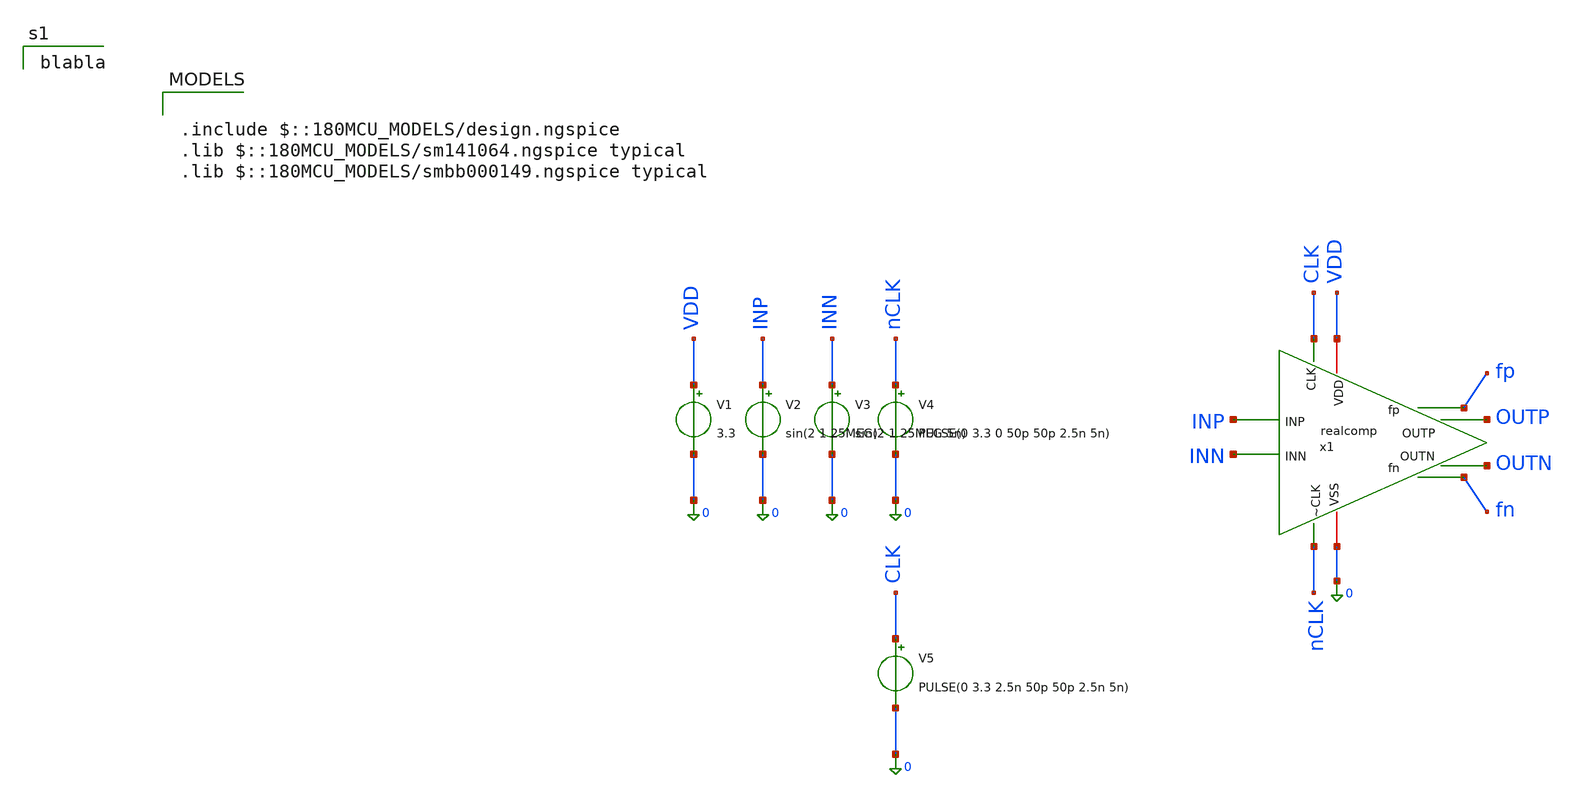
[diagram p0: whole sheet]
** sch_path: analog/blocks/Double_Tail_Comparator/realcomptest.sch
**.subckt realcomptest
V1 VDD 0 3.3
V2 INP 0 sin(2 1 25MEG)
V3 INN 0 sin(2 1 25MEG 5n)
V4 nCLK 0 PULSE(0 3.3 0 50p 50p 2.5n 5n)
V5 CLK 0 PULSE(0 3.3 2.5n 50p 50p 2.5n 5n)
x1 nCLK OUTN OUTP CLK VDD 0 fp fn INP INN realcomp
**** begin user architecture code

blabla


.include $::180MCU_MODELS/design.ngspice
.lib $::180MCU_MODELS/sm141064.ngspice typical
.lib $::180MCU_MODELS/smbb000149.ngspice typical

**** end user architecture code
**.ends

* expanding   symbol:  realcomp.sym # of pins=10
** sym_path: analog/blocks/Double_Tail_Comparator/realcomp.sym
** sch_path: analog/blocks/Double_Tail_Comparator/realcomp.sch
.subckt realcomp ~CLK OUTN OUTP CLK VDD VSS fp fn INP INN
*.ipin INN
*.ipin INP
*.ipin CLK
*.iopin VSS
*.iopin VDD
*.opin OUTP
*.opin OUTN
*.ipin ~CLK
*.opin fn
*.opin fp
XM1 net1 ~CLK VDD VDD pfet_03v3 L=0.28u W=1.1u nf=1 ad='int((nf+1)/2) * W/nf * 0.18u' as='int((nf+2)/2) * W/nf * 0.18u'
+ pd='2*int((nf+1)/2) * (W/nf + 0.18u)' ps='2*int((nf+2)/2) * (W/nf + 0.18u)' nrd='0.18u / W' nrs='0.18u / W'
+ sa=0 sb=0 sd=0 m=1
XM2 OUTP OUTN net1 VDD pfet_03v3 L=0.28u W=0.44u nf=1 ad='int((nf+1)/2) * W/nf * 0.18u' as='int((nf+2)/2) * W/nf * 0.18u'
+ pd='2*int((nf+1)/2) * (W/nf + 0.18u)' ps='2*int((nf+2)/2) * (W/nf + 0.18u)' nrd='0.18u / W' nrs='0.18u / W'
+ sa=0 sb=0 sd=0 m=1
XM3 fn fp VDD VDD pfet_03v3 L=0.28u W=0.66u nf=1 ad='int((nf+1)/2) * W/nf * 0.18u' as='int((nf+2)/2) * W/nf * 0.18u'
+ pd='2*int((nf+1)/2) * (W/nf + 0.18u)' ps='2*int((nf+2)/2) * (W/nf + 0.18u)' nrd='0.18u / W' nrs='0.18u / W'
+ sa=0 sb=0 sd=0 m=1
XM4 fp CLK VDD VDD pfet_03v3 L=0.28u W=0.22u nf=1 ad='int((nf+1)/2) * W/nf * 0.18u' as='int((nf+2)/2) * W/nf * 0.18u'
+ pd='2*int((nf+1)/2) * (W/nf + 0.18u)' ps='2*int((nf+2)/2) * (W/nf + 0.18u)' nrd='0.18u / W' nrs='0.18u / W'
+ sa=0 sb=0 sd=0 m=1
XM5 OUTN OUTP net1 VDD pfet_03v3 L=0.28u W=0.44u nf=1 ad='int((nf+1)/2) * W/nf * 0.18u' as='int((nf+2)/2) * W/nf * 0.18u'
+ pd='2*int((nf+1)/2) * (W/nf + 0.18u)' ps='2*int((nf+2)/2) * (W/nf + 0.18u)' nrd='0.18u / W' nrs='0.18u / W'
+ sa=0 sb=0 sd=0 m=1
XM8 OUTP OUTN VSS VSS nfet_03v3 L=0.28u W=0.44u nf=1 ad='int((nf+1)/2) * W/nf * 0.18u' as='int((nf+2)/2) * W/nf * 0.18u'
+ pd='2*int((nf+1)/2) * (W/nf + 0.18u)' ps='2*int((nf+2)/2) * (W/nf + 0.18u)' nrd='0.18u / W' nrs='0.18u / W'
+ sa=0 sb=0 sd=0 m=1
XM15 OUTN fp VSS VSS nfet_03v3 L=0.28u W=0.22u nf=1 ad='int((nf+1)/2) * W/nf * 0.18u' as='int((nf+2)/2) * W/nf * 0.18u'
+ pd='2*int((nf+1)/2) * (W/nf + 0.18u)' ps='2*int((nf+2)/2) * (W/nf + 0.18u)' nrd='0.18u / W' nrs='0.18u / W'
+ sa=0 sb=0 sd=0 m=1
XM11 OUTP fn VSS VSS nfet_03v3 L=0.28u W=0.22u nf=1 ad='int((nf+1)/2) * W/nf * 0.18u' as='int((nf+2)/2) * W/nf * 0.18u'
+ pd='2*int((nf+1)/2) * (W/nf + 0.18u)' ps='2*int((nf+2)/2) * (W/nf + 0.18u)' nrd='0.18u / W' nrs='0.18u / W'
+ sa=0 sb=0 sd=0 m=1
XM13 fp INN net2 VSS nfet_03v3 L=0.28u W=2.1u nf=1 ad='int((nf+1)/2) * W/nf * 0.18u' as='int((nf+2)/2) * W/nf * 0.18u'
+ pd='2*int((nf+1)/2) * (W/nf + 0.18u)' ps='2*int((nf+2)/2) * (W/nf + 0.18u)' nrd='0.18u / W' nrs='0.18u / W'
+ sa=0 sb=0 sd=0 m=1
XM14 net2 fn net4 VSS nfet_03v3 L=0.28u W=0.22u nf=1 ad='int((nf+1)/2) * W/nf * 0.18u' as='int((nf+2)/2) * W/nf * 0.18u'
+ pd='2*int((nf+1)/2) * (W/nf + 0.18u)' ps='2*int((nf+2)/2) * (W/nf + 0.18u)' nrd='0.18u / W' nrs='0.18u / W'
+ sa=0 sb=0 sd=0 m=1
XM16 net4 CLK VSS VSS nfet_03v3 L=0.28u W=0.22u nf=1 ad='int((nf+1)/2) * W/nf * 0.18u' as='int((nf+2)/2) * W/nf * 0.18u'
+ pd='2*int((nf+1)/2) * (W/nf + 0.18u)' ps='2*int((nf+2)/2) * (W/nf + 0.18u)' nrd='0.18u / W' nrs='0.18u / W'
+ sa=0 sb=0 sd=0 m=1
XM9 OUTN OUTP VSS VSS nfet_03v3 L=0.28u W=0.44u nf=1 ad='int((nf+1)/2) * W/nf * 0.18u' as='int((nf+2)/2) * W/nf * 0.18u'
+ pd='2*int((nf+1)/2) * (W/nf + 0.18u)' ps='2*int((nf+2)/2) * (W/nf + 0.18u)' nrd='0.18u / W' nrs='0.18u / W'
+ sa=0 sb=0 sd=0 m=1
XM6 fp fn VDD VDD pfet_03v3 L=0.28u W=0.66u nf=1 ad='int((nf+1)/2) * W/nf * 0.18u' as='int((nf+2)/2) * W/nf * 0.18u'
+ pd='2*int((nf+1)/2) * (W/nf + 0.18u)' ps='2*int((nf+2)/2) * (W/nf + 0.18u)' nrd='0.18u / W' nrs='0.18u / W'
+ sa=0 sb=0 sd=0 m=1
XM7 fn CLK VDD VDD pfet_03v3 L=0.28u W=0.22u nf=1 ad='int((nf+1)/2) * W/nf * 0.18u' as='int((nf+2)/2) * W/nf * 0.18u'
+ pd='2*int((nf+1)/2) * (W/nf + 0.18u)' ps='2*int((nf+2)/2) * (W/nf + 0.18u)' nrd='0.18u / W' nrs='0.18u / W'
+ sa=0 sb=0 sd=0 m=1
XM10 fn INP net3 VSS nfet_03v3 L=0.28u W=2.1u nf=1 ad='int((nf+1)/2) * W/nf * 0.18u' as='int((nf+2)/2) * W/nf * 0.18u'
+ pd='2*int((nf+1)/2) * (W/nf + 0.18u)' ps='2*int((nf+2)/2) * (W/nf + 0.18u)' nrd='0.18u / W' nrs='0.18u / W'
+ sa=0 sb=0 sd=0 m=1
XM12 net3 fp net4 VSS nfet_03v3 L=0.28u W=0.22u nf=1 ad='int((nf+1)/2) * W/nf * 0.18u' as='int((nf+2)/2) * W/nf * 0.18u'
+ pd='2*int((nf+1)/2) * (W/nf + 0.18u)' ps='2*int((nf+2)/2) * (W/nf + 0.18u)' nrd='0.18u / W' nrs='0.18u / W'
+ sa=0 sb=0 sd=0 m=1
.ends

.end
